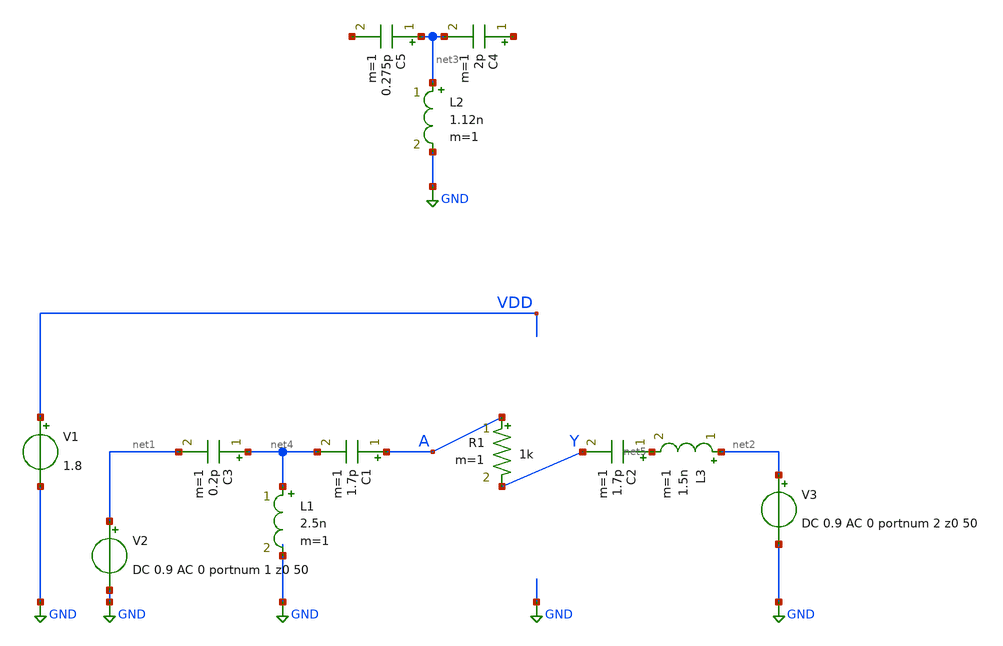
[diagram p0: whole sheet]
** sch_path: xschem/dumb_amp_2.sch
**.subckt dumb_amp_2
V1 VDD GND 1.8
V3 net2 GND DC 0.9 AC 0 portnum 2 z0 50
V2 net1 GND DC 0.9 AC 0 portnum 1 z0 50
C1 A net4 1.7p m=1
C2 net5 Y 1.7p m=1
C4 net6 net3 2p m=1
C5 net3 net7 0.275p m=1
L2 net3 GND 1.12n m=1
C3 net4 net1 0.2p m=1
L1 net4 GND 2.5n m=1
L3 net2 net5 1.5n m=1
R1 A Y 1k m=1
**** begin user architecture code
.lib $::SKYWATER_MODELS/sky130.lib.spice tt
* .include $::PDKPATH/libs.ref/sky130_fd_sc_hvl/spice/sky130_fd_sc_hvl.spice


.subckt DUT_PEX A Y VHI VLO
R0 A Y sky130_fd_pr__res_generic_po w=460000u l=6.54e+06u
X0 Y A VHI VHI sky130_fd_pr__pfet_01v8 ad=0p pd=0u as=0p ps=0u w=4e+06u l=150000u
X1 VHI A Y VHI sky130_fd_pr__pfet_01v8 ad=0p pd=0u as=0p ps=0u w=4e+06u l=150000u
X2 Y A VHI VHI sky130_fd_pr__pfet_01v8 ad=0p pd=0u as=0p ps=0u w=4e+06u l=150000u
X3 Y A VHI VHI sky130_fd_pr__pfet_01v8 ad=0p pd=0u as=0p ps=0u w=4e+06u l=150000u
X4 Y A VHI VHI sky130_fd_pr__pfet_01v8 ad=0p pd=0u as=0p ps=0u w=4e+06u l=150000u
X5 VHI A Y VHI sky130_fd_pr__pfet_01v8 ad=0p pd=0u as=0p ps=0u w=4e+06u l=150000u
X6 VHI A Y VHI sky130_fd_pr__pfet_01v8 ad=0p pd=0u as=0p ps=0u w=4e+06u l=150000u
X7 VHI A Y VHI sky130_fd_pr__pfet_01v8 ad=0p pd=0u as=0p ps=0u w=4e+06u l=150000u
X8 VHI A Y VHI sky130_fd_pr__pfet_01v8 ad=0p pd=0u as=0p ps=0u w=4e+06u l=150000u
X9 Y A VHI VHI sky130_fd_pr__pfet_01v8 ad=0p pd=0u as=0p ps=0u w=4e+06u l=150000u
X10 VHI A Y VHI sky130_fd_pr__pfet_01v8 ad=0p pd=0u as=0p ps=0u w=4e+06u l=150000u
X11 Y A VHI VHI sky130_fd_pr__pfet_01v8 ad=0p pd=0u as=0p ps=0u w=4e+06u l=150000u
X12 VHI A Y VHI sky130_fd_pr__pfet_01v8 ad=0p pd=0u as=0p ps=0u w=4e+06u l=150000u
X13 Y A VHI VHI sky130_fd_pr__pfet_01v8 ad=0p pd=0u as=0p ps=0u w=4e+06u l=150000u
X14 Y A VHI VHI sky130_fd_pr__pfet_01v8 ad=0p pd=0u as=0p ps=0u w=4e+06u l=150000u
X15 Y A VHI VHI sky130_fd_pr__pfet_01v8 ad=0p pd=0u as=0p ps=0u w=4e+06u l=150000u
X16 VHI A Y VHI sky130_fd_pr__pfet_01v8 ad=0p pd=0u as=0p ps=0u w=4e+06u l=150000u
X17 VHI A Y VHI sky130_fd_pr__pfet_01v8 ad=0p pd=0u as=0p ps=0u w=4e+06u l=150000u
X18 VHI A Y VHI sky130_fd_pr__pfet_01v8 ad=0p pd=0u as=0p ps=0u w=4e+06u l=150000u
X19 Y A VHI VHI sky130_fd_pr__pfet_01v8 ad=0p pd=0u as=0p ps=0u w=4e+06u l=150000u
X20 Y A VHI VHI sky130_fd_pr__pfet_01v8 ad=0p pd=0u as=0p ps=0u w=4e+06u l=150000u
X21 VHI A Y VHI sky130_fd_pr__pfet_01v8 ad=0p pd=0u as=0p ps=0u w=4e+06u l=150000u
X22 VHI A Y VHI sky130_fd_pr__pfet_01v8 ad=0p pd=0u as=0p ps=0u w=4e+06u l=150000u
X23 VHI A Y VHI sky130_fd_pr__pfet_01v8 ad=0p pd=0u as=0p ps=0u w=4e+06u l=150000u
X24 Y A VHI VHI sky130_fd_pr__pfet_01v8 ad=0p pd=0u as=0p ps=0u w=4e+06u l=150000u
X25 Y A VHI VHI sky130_fd_pr__pfet_01v8 ad=0p pd=0u as=0p ps=0u w=4e+06u l=150000u
X26 Y A VHI VHI sky130_fd_pr__pfet_01v8 ad=0p pd=0u as=0p ps=0u w=4e+06u l=150000u
X27 Y A VHI VHI sky130_fd_pr__pfet_01v8 ad=0p pd=0u as=0p ps=0u w=4e+06u l=150000u
X28 Y A VHI VHI sky130_fd_pr__pfet_01v8 ad=0p pd=0u as=0p ps=0u w=4e+06u l=150000u
X29 VHI A Y VHI sky130_fd_pr__pfet_01v8 ad=0p pd=0u as=0p ps=0u w=4e+06u l=150000u
X30 VHI A Y VHI sky130_fd_pr__pfet_01v8 ad=0p pd=0u as=0p ps=0u w=4e+06u l=150000u
X31 VHI A Y VHI sky130_fd_pr__pfet_01v8 ad=0p pd=0u as=0p ps=0u w=4e+06u l=150000u
X32 VLO A Y VLO sky130_fd_pr__nfet_01v8 ad=0p pd=0u as=0p ps=0u w=4e+06u l=150000u
X33 Y A VLO VLO sky130_fd_pr__nfet_01v8 ad=0p pd=0u as=0p ps=0u w=4e+06u l=150000u
X34 Y A VLO VLO sky130_fd_pr__nfet_01v8 ad=0p pd=0u as=0p ps=0u w=4e+06u l=150000u
X35 Y A VLO VLO sky130_fd_pr__nfet_01v8 ad=0p pd=0u as=0p ps=0u w=4e+06u l=150000u
X36 VLO A Y VLO sky130_fd_pr__nfet_01v8 ad=0p pd=0u as=0p ps=0u w=4e+06u l=150000u
X37 Y A VLO VLO sky130_fd_pr__nfet_01v8 ad=0p pd=0u as=0p ps=0u w=4e+06u l=150000u
X38 VLO A Y VLO sky130_fd_pr__nfet_01v8 ad=0p pd=0u as=0p ps=0u w=4e+06u l=150000u
X39 Y A VLO VLO sky130_fd_pr__nfet_01v8 ad=0p pd=0u as=0p ps=0u w=4e+06u l=150000u
X40 Y A VLO VLO sky130_fd_pr__nfet_01v8 ad=0p pd=0u as=0p ps=0u w=4e+06u l=150000u
X41 VLO A Y VLO sky130_fd_pr__nfet_01v8 ad=0p pd=0u as=0p ps=0u w=4e+06u l=150000u
X42 VLO A Y VLO sky130_fd_pr__nfet_01v8 ad=0p pd=0u as=0p ps=0u w=4e+06u l=150000u
X43 VLO A Y VLO sky130_fd_pr__nfet_01v8 ad=0p pd=0u as=0p ps=0u w=4e+06u l=150000u
X44 Y A VLO VLO sky130_fd_pr__nfet_01v8 ad=0p pd=0u as=0p ps=0u w=4e+06u l=150000u
X45 Y A VLO VLO sky130_fd_pr__nfet_01v8 ad=0p pd=0u as=0p ps=0u w=4e+06u l=150000u
X46 VLO A Y VLO sky130_fd_pr__nfet_01v8 ad=0p pd=0u as=0p ps=0u w=4e+06u l=150000u
X47 VLO A Y VLO sky130_fd_pr__nfet_01v8 ad=0p pd=0u as=0p ps=0u w=4e+06u l=150000u
C0 VLO Y 37.95fF
C1 VLO VHI 5.31fF
C2 VLO A 10.01fF
C3 Y VHI 74.69fF
C4 A Y 21.97fF
C5 A VHI 23.59fF
C6 VLO 0 8.21fF
C7 Y 0 2.50fF
C8 A 0 2.76fF
C9 VHI 0 14.48fF
.ends

XDUT A Y VDD GND DUT_PEX

.sp dec 1000 1e9 10e9 1


* .ac dec 1000 0.01e9 100e9
.control
run
display
let z11=50*(1+s_1_1)/(1-s_1_1)
let z22=50*(1+s_2_2)/(1-s_2_2)
let S11 = S_1_1
let S21 = S_2_1
let S12 = S_1_2
let S22 = S_2_2

* Stability
let delta=S11*S22-S12*S21
let K    = (1-mag(S11)^2-mag(S22)^2+mag(delta)^2)/(2*mag(S12*S21))
let mu   = (1-mag(S11)^2)/(mag(S22-conj(S11)*delta)+mag(S21*S12))
* plot real(z11) real(z22)
* plot imag(z11) imag(z22)
plot db(S_1_1) db(S_2_2) db(S_2_1)
*
plot db(K)
plot mag(delta)
plot db(mu)
plot NF NFmin
.endc


**** end user architecture code
**.ends
.GLOBAL GND
.end
